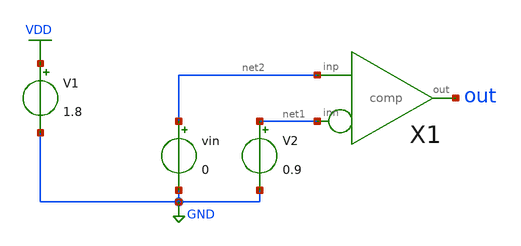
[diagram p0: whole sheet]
** sch_path: xschem/comp_tb.sch
**.subckt comp_tb
V1 VDD GND 1.8
V2 net1 GND 0.9
vin net2 GND 0
X1 net2 net1 out comp
**** begin user architecture code


.option wnflag=1
.lib /usr/local/share/pdk/sky130A/libs.tech/ngspice/sky130.lib.spice tt
.dc vin 0 1.8 0.01
.save all


**** end user architecture code
**.ends

* expanding   symbol:  comp.sym # of pins=3
** sym_path: xschem/comp.sym
** sch_path: xschem/comp.sch
.subckt comp inp inn out
*.ipin inp
*.ipin inn
*.opin out
XM1 outn inp net2 GND sky130_fd_pr__nfet_01v8 L=0.15 W=1 nf=1 ad='int((1 + 1)/2) * 1 / 1 * 0.29' as='int((1 + 2)/2) * 1 / 1 * 0.29'
+ pd='2*int((1 + 1)/2) * (1 / 1 + 0.29)' ps='2*int((1 + 2)/2) * (1 / 1 + 0.29)' nrd='0.29 / 1 ' nrs='0.29 / 1 '
+ sa=0 sb=0 sd=0 mult=1 m=1
XM2 outn net1 VDD VDD sky130_fd_pr__pfet_01v8 L=0.15 W=1 nf=1 ad='int((1 + 1)/2) * 1 / 1 * 0.29' as='int((1 + 2)/2) * 1 / 1 * 0.29'
+ pd='2*int((1 + 1)/2) * (1 / 1 + 0.29)' ps='2*int((1 + 2)/2) * (1 / 1 + 0.29)' nrd='0.29 / 1 ' nrs='0.29 / 1 '
+ sa=0 sb=0 sd=0 mult=1 m=1
XM3 net1 net1 VDD VDD sky130_fd_pr__pfet_01v8 L=0.15 W=1 nf=1 ad='int((1 + 1)/2) * 1 / 1 * 0.29' as='int((1 + 2)/2) * 1 / 1 * 0.29'
+ pd='2*int((1 + 1)/2) * (1 / 1 + 0.29)' ps='2*int((1 + 2)/2) * (1 / 1 + 0.29)' nrd='0.29 / 1 ' nrs='0.29 / 1 '
+ sa=0 sb=0 sd=0 mult=1 m=1
XM4 net1 inn net2 GND sky130_fd_pr__nfet_01v8 L=0.15 W=1 nf=1 ad='int((1 + 1)/2) * 1 / 1 * 0.29' as='int((1 + 2)/2) * 1 / 1 * 0.29'
+ pd='2*int((1 + 1)/2) * (1 / 1 + 0.29)' ps='2*int((1 + 2)/2) * (1 / 1 + 0.29)' nrd='0.29 / 1 ' nrs='0.29 / 1 '
+ sa=0 sb=0 sd=0 mult=1 m=1
XM5 net2 net3 GND GND sky130_fd_pr__nfet_01v8 L=0.15 W=1 nf=1 ad='int((1 + 1)/2) * 1 / 1 * 0.29' as='int((1 + 2)/2) * 1 / 1 * 0.29'
+ pd='2*int((1 + 1)/2) * (1 / 1 + 0.29)' ps='2*int((1 + 2)/2) * (1 / 1 + 0.29)' nrd='0.29 / 1 ' nrs='0.29 / 1 '
+ sa=0 sb=0 sd=0 mult=1 m=1
XM6 net3 net3 GND GND sky130_fd_pr__nfet_01v8 L=0.15 W=1 nf=1 ad='int((1 + 1)/2) * 1 / 1 * 0.29' as='int((1 + 2)/2) * 1 / 1 * 0.29'
+ pd='2*int((1 + 1)/2) * (1 / 1 + 0.29)' ps='2*int((1 + 2)/2) * (1 / 1 + 0.29)' nrd='0.29 / 1 ' nrs='0.29 / 1 '
+ sa=0 sb=0 sd=0 mult=1 m=1
XR1 net3 VDD res100k
XM7 out outn GND GND sky130_fd_pr__nfet_01v8 L=0.15 W=1 nf=1 ad='int((1 + 1)/2) * 1 / 1 * 0.29' as='int((1 + 2)/2) * 1 / 1 * 0.29'
+ pd='2*int((1 + 1)/2) * (1 / 1 + 0.29)' ps='2*int((1 + 2)/2) * (1 / 1 + 0.29)' nrd='0.29 / 1 ' nrs='0.29 / 1 '
+ sa=0 sb=0 sd=0 mult=1 m=1
XM8 out outn VDD VDD sky130_fd_pr__pfet_01v8 L=0.15 W=1 nf=1 ad='int((1 + 1)/2) * 1 / 1 * 0.29' as='int((1 + 2)/2) * 1 / 1 * 0.29'
+ pd='2*int((1 + 1)/2) * (1 / 1 + 0.29)' ps='2*int((1 + 2)/2) * (1 / 1 + 0.29)' nrd='0.29 / 1 ' nrs='0.29 / 1 '
+ sa=0 sb=0 sd=0 mult=1 m=1
.ends


* expanding   symbol:  res100k.sym # of pins=2
** sym_path: xschem/res100k.sym
** sch_path: xschem/res100k.sch
.subckt res100k bot top
*.iopin top
*.iopin bot
XR1 net1 top GND sky130_fd_pr__res_xhigh_po_0p35 L=3.5 mult=1 m=1
XR2 net2 net1 GND sky130_fd_pr__res_xhigh_po_0p35 L=3.5 mult=1 m=1
XR3 net3 net2 GND sky130_fd_pr__res_xhigh_po_0p35 L=3.5 mult=1 m=1
XR4 net4 net3 GND sky130_fd_pr__res_xhigh_po_0p35 L=3.5 mult=1 m=1
XR5 bot net4 GND sky130_fd_pr__res_xhigh_po_0p35 L=3.5 mult=1 m=1
.ends

.GLOBAL GND
.GLOBAL VDD
.end
